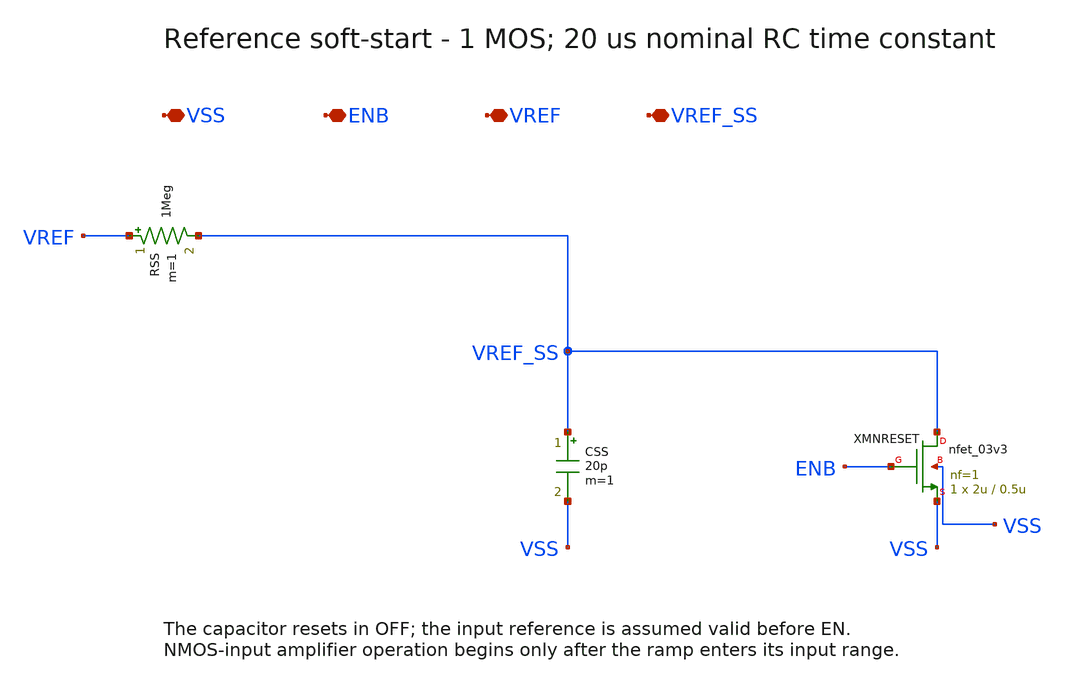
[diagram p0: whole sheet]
** sch_path: schematics/ldo_softstart.sch
**.subckt ldo_softstart VSS ENB VREF VREF_SS
*.iopin VSS
*.iopin ENB
*.iopin VREF
*.iopin VREF_SS
RSS VREF VREF_SS 1Meg m=1
CSS VREF_SS VSS 20p m=1
XMNRESET VREF_SS ENB VSS VSS nfet_03v3 L=0.5u W=2u nf=1 ad='int((nf+1)/2)*W/nf*0.18u' as='int((nf+2)/2)*W/nf*0.18u'
+ pd='2*int((nf+1)/2)*(W/nf+0.18u)' ps='2*int((nf+2)/2)*(W/nf+0.18u)' nrd='0.18u/W' nrs='0.18u/W' sa=0
+ sb=0 sd=0 m=1 par=1
**.ends
.end
